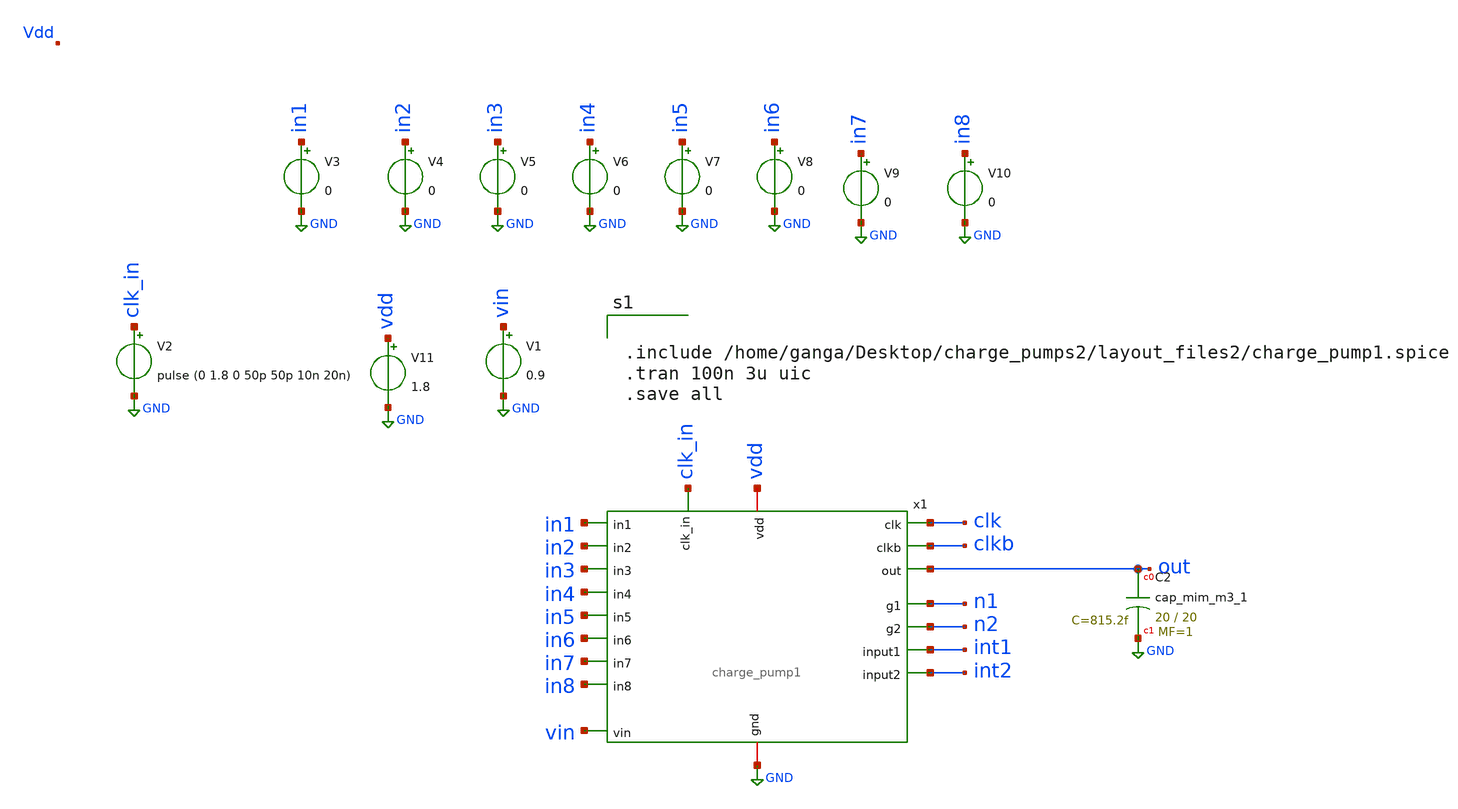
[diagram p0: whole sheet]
** sch_path: xschem/charge_pumps2/CP1_post_layout2.sch
**.subckt CP1_post_layout2
V1 vin GND 0.9
V2 clk_in GND pulse (0 1.8 0 50p 50p 10n 20n)
V3 in1 GND 0
V4 in2 GND 0
V5 in3 GND 0
V6 in4 GND 0
V7 in5 GND 0
V8 in6 GND 0
V9 in7 GND 0
V10 in8 GND 0
V11 vdd GND 1.8
XC2 out GND sky130_fd_pr__cap_mim_m3_1 W=20 L=20 MF=1 m=1
x1 clk_in n2 vin n1 int1 int2 vdd GND out clk clkb in1 in3 in2 in4 in5 in6 in7 in8 charge_pump1
**** begin user architecture code

** opencircuitdesign pdks install
.lib $::SKYWATER_MODELS/sky130.lib.spice tt




.include /home/ganga/Desktop/charge_pumps2/layout_files2/charge_pump1.spice
.tran 100n 3u uic
.save all


**** end user architecture code
**.ends
.GLOBAL GND
.end
